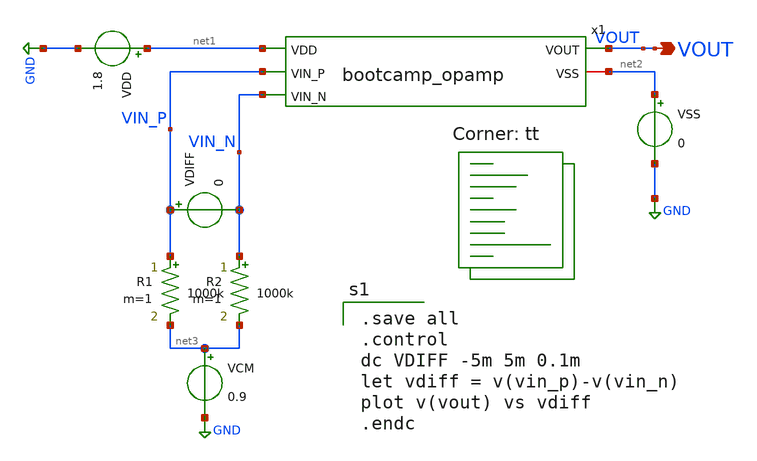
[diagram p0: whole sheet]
** sch_path: analog/build/schematic/tb_dc_analysis.sch
**.subckt tb_dc_analysis VOUT
*.opin VOUT
VDD net1 GND 1.8
VSS net2 GND 0
VDIFF VIN_P VIN_N 0
R1 VIN_P net3 1000k m=1
R2 VIN_N net3 1000k m=1
VCM net3 GND 0.9
x1 net1 VOUT VIN_P VIN_N net2 bootcamp_opamp
**** begin user architecture code

.save all
.control
dc VDIFF -5m 5m 0.1m
let vdiff = v(vin_p)-v(vin_n)
plot v(vout) vs vdiff
.endc

.lib $::SKYWATER_MODELS/sky130.lib.spice tt
**** end user architecture code
**.ends

* expanding   symbol:  bootcamp_opamp.sym # of pins=5
** sym_path: analog/schematics/bootcamp_opamp.sym
** sch_path: analog/schematics/bootcamp_opamp.sch
.subckt bootcamp_opamp VDD VOUT VIN_P VIN_N VSS
*.ipin VIN_P
*.ipin VIN_N
*.iopin VSS
*.opin VOUT
*.ipin VDD
XM1 net1 net1 VDD VDD sky130_fd_pr__pfet_01v8 L=0.5 W=10 nf=1 ad='int((nf+1)/2) * W/nf * 0.29' as='int((nf+2)/2) * W/nf * 0.29'
+ pd='2*int((nf+1)/2) * (W/nf + 0.29)' ps='2*int((nf+2)/2) * (W/nf + 0.29)' nrd='0.29 / W' nrs='0.29 / W'
+ sa=0 sb=0 sd=0 mult=1 m=1
XM2 VOUT net1 VDD VDD sky130_fd_pr__pfet_01v8 L=0.5 W=10 nf=1 ad='int((nf+1)/2) * W/nf * 0.29' as='int((nf+2)/2) * W/nf * 0.29'
+ pd='2*int((nf+1)/2) * (W/nf + 0.29)' ps='2*int((nf+2)/2) * (W/nf + 0.29)' nrd='0.29 / W' nrs='0.29 / W'
+ sa=0 sb=0 sd=0 mult=1 m=1
XM3 VOUT VOUT VDD VDD sky130_fd_pr__pfet_01v8 L=0.5 W=10 nf=1 ad='int((nf+1)/2) * W/nf * 0.29' as='int((nf+2)/2) * W/nf * 0.29'
+ pd='2*int((nf+1)/2) * (W/nf + 0.29)' ps='2*int((nf+2)/2) * (W/nf + 0.29)' nrd='0.29 / W' nrs='0.29 / W'
+ sa=0 sb=0 sd=0 mult=1 m=1
XM4 net1 VIN_P net2 VSS sky130_fd_pr__nfet_01v8 L=0.5 W=16 nf=1 ad='int((nf+1)/2) * W/nf * 0.29' as='int((nf+2)/2) * W/nf * 0.29'
+ pd='2*int((nf+1)/2) * (W/nf + 0.29)' ps='2*int((nf+2)/2) * (W/nf + 0.29)' nrd='0.29 / W' nrs='0.29 / W'
+ sa=0 sb=0 sd=0 mult=1 m=1
XM5 VOUT VIN_N net2 VSS sky130_fd_pr__nfet_01v8 L=0.5 W=16 nf=1 ad='int((nf+1)/2) * W/nf * 0.29' as='int((nf+2)/2) * W/nf * 0.29'
+ pd='2*int((nf+1)/2) * (W/nf + 0.29)' ps='2*int((nf+2)/2) * (W/nf + 0.29)' nrd='0.29 / W' nrs='0.29 / W'
+ sa=0 sb=0 sd=0 mult=1 m=1
XM6 net2 net3 VSS VSS sky130_fd_pr__nfet_01v8 L=0.8 W=4 nf=1 ad='int((nf+1)/2) * W/nf * 0.29' as='int((nf+2)/2) * W/nf * 0.29'
+ pd='2*int((nf+1)/2) * (W/nf + 0.29)' ps='2*int((nf+2)/2) * (W/nf + 0.29)' nrd='0.29 / W' nrs='0.29 / W'
+ sa=0 sb=0 sd=0 mult=1 m=1
XM7 net3 net3 VSS VSS sky130_fd_pr__nfet_01v8 L=0.8 W=4 nf=1 ad='int((nf+1)/2) * W/nf * 0.29' as='int((nf+2)/2) * W/nf * 0.29'
+ pd='2*int((nf+1)/2) * (W/nf + 0.29)' ps='2*int((nf+2)/2) * (W/nf + 0.29)' nrd='0.29 / W' nrs='0.29 / W'
+ sa=0 sb=0 sd=0 mult=1 m=1
XM8 VOUT VSS VSS VSS sky130_fd_pr__nfet_01v8 L=0.8 W=4 nf=1 ad='int((nf+1)/2) * W/nf * 0.29' as='int((nf+2)/2) * W/nf * 0.29'
+ pd='2*int((nf+1)/2) * (W/nf + 0.29)' ps='2*int((nf+2)/2) * (W/nf + 0.29)' nrd='0.29 / W' nrs='0.29 / W'
+ sa=0 sb=0 sd=0 mult=1 m=1
XC1 VOUT VSS sky130_fd_pr__cap_mim_m3_1 W=1 L=1 MF=1 m=1
R2 net3 VDD sky130_fd_pr__res_generic_m1 W=1 L=1 m=1
.ends

.GLOBAL GND
.end
